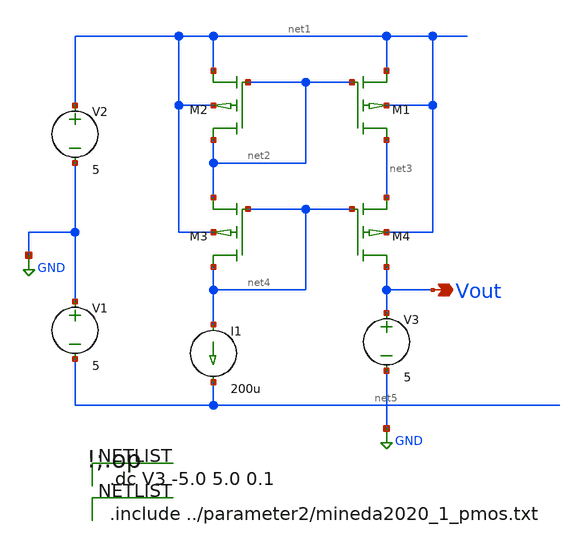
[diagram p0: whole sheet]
** sch_path: currentsource_test14umcascode.sch
**.subckt currentsource_test14umcascode Vout
*.opin Vout
V1 GND net5 5
M1 net3 net2 net1 net1 YSS_PMOS w=14u l=14u as=0 ps=0 ad=0 pd=0 m=20
V2 net1 GND 5
I1 net4 net5 200u
M2 net2 net2 net1 net1 YSS_PMOS w=14u l=14u as=0 ps=0 ad=0 pd=0 m=20
V3 Vout GND 5
M3 net4 net4 net2 net1 YSS_PMOS w=14u l=14u as=0 ps=0 ad=0 pd=0 m=20
M4 Vout net4 net3 net1 YSS_PMOS w=14u l=14u as=0 ps=0 ad=0 pd=0 m=20
**** begin user architecture code

.dc V3 -5.0 5.0 0.1


.include ../parameter2/mineda2020_1_pmos.txt

**** end user architecture code
**.ends
.GLOBAL GND
.end
